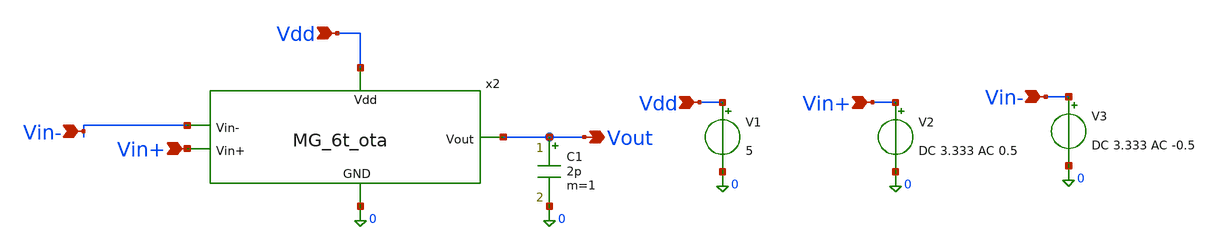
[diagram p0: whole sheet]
** sch_path: MG_6T_OTA/MG_6t_ota_testbench.sch
**.subckt MG_6t_ota_testbench Vdd Vin+ Vin- Vdd Vin+ Vin- Vout
*.ipin Vdd
*.ipin Vin+
*.ipin Vin-
*.ipin Vdd
*.ipin Vin+
*.ipin Vin-
*.opin Vout
V1 Vdd 0 5
V2 Vin+ 0 DC 3.333 AC 0.5
V3 Vin- 0 DC 3.333 AC -0.5
C1 Vout 0 2p m=1
x2 Vdd Vout Vin- Vin+ 0 MG_6t_ota
**** begin user architecture code



.include /foss/pdks/gf180mcuD/libs.tech/ngspice/design.ngspice
.lib /foss/pdks/gf180mcuD/libs.tech/ngspice/sm141064.ngspice typical
.lib /foss/pdks/gf180mcuD/libs.tech/ngspice/sm141064.ngspice res_typical
.lib /foss/pdks/gf180mcuD/libs.tech/ngspice/sm141064.ngspice moscap_typical
.lib /foss/pdks/gf180mcuD/libs.tech/ngspice/sm141064.ngspice diode_typical

.control
 save all
  op
  print all

  ac dec 10 1 1G
  meas ac dc_gain MAX vdb(Vout)
  meas ac ugbw WHEN vdb(Vout)=0 FALL=1
  let phase_deg = (180/PI)*vp(Vout)
  plot vdb(Vout)
  plot phase_deg
.endc


*.control
  *save all
  *op

  * ==========================================
  * 1. DIFFERENTIAL RUN (Adm & Noise)
  * ==========================================
  *alter v2 ac = 1
  *alter v3 ac = -1 ; Set this to 0 if v3 is just a DC reference

  *ac dec 20 1 1G
  *setplot ac1

  *let gain_db = vdb(vout)
  *let phase_deg = (180/PI) * ph(vout)
  *meas ac dc_gain MAX gain_db

  * Run Noise Analysis on the Differential Setup
  *noise v(vout) v2 dec 20 1 1G

  * ==========================================
  * 2. COMMON-MODE RUN (Acm)
  * ==========================================
  * Force both inputs to swing exactly the same way
  *alter v2 ac = 1
  *alter v3 ac = 1

  *ac dec 20 1 1G
  *setplot ac2
  *let cm_gain_db = vdb(vout)

  * ==========================================
  * 3. CMRR CALCULATION
  * ==========================================
  * CMRR = Differential Gain - Common Mode Gain
  *let cmrr_db = ac1.gain_db - ac2.cm_gain_db
  *meas ac max_cmrr MAX cmrr_db

  *print ac1.dc_gain max_cmrr

  * Plot everything together
  *plot ac1.gain_db ac2.cm_gain_db title 'Diff Gain vs CM Gain (dB)'
  *plot cmrr_db title 'CMRR (dB)'

  * =========================================
  * 4. NOISE CALCULATION
  * =========================================

  * Syntax: noise v(output_node) input_source dec points fstart fstop
  *noise v(vout) v2 dec 20 1 1G

  * ngspice creates 'noise1' for spectral density and 'noise2' for total noise
  *setplot noise1

  * Plot spectral densities (V/sqrt(Hz))
  *plot inoise_spectrum title 'Input Referred Noise Density'
  *plot onoise_spectrum title 'Output Referred Noise Density'

  * Calculate and print total integrated input RMS noise over the bandwidth
  *let total_in_noise = sqrt(integ(inoise_spectrum^2))
  *print total_in_noise


*.endc

*.include /foss/pdks/gf180mcuD/libs.tech/ngspice/design.ngspice

* MUST be defined here exactly as 1
*.param sw_stat_global=1
*.param sw_stat_mismatch=1

*.lib /foss/pdks/gf180mcuD/libs.tech/ngspice/sm141064.ngspice statistical
*.lib /foss/pdks/gf180mcuD/libs.tech/ngspice/sm141064.ngspice res_statistical
*.lib /foss/pdks/gf180mcuD/libs.tech/ngspice/sm141064.ngspice moscap_typical
*.lib /foss/pdks/gf180mcuD/libs.tech/ngspice/sm141064.ngspice diode_typical

*.control
*  let mc_runs = 50
*  let run_idx = 1

*  echo Run_Number DC_Gain_dB UGBW_Hz Phase_Margin_Deg > mc_results.txt

*  while run_idx <= mc_runs

    * 1. FLUSH THE CACHE: Turn off MC and reset
    * This forces NGSPICE to recognize a physical state change
*    alterparam sw_stat_global = 0
*    alterparam sw_stat_mismatch = 0
*    reset

    * 2. ROLL NEW DICE: Change seed, turn MC back on exactly to 1, and reset
    * Because the state changed from 0 -> 1, NGSPICE is forced to re-evaluate
    * the agauss() functions with the new seed!
*    setseed $&run_idx
*    alterparam sw_stat_global = 1
*    alterparam sw_stat_mismatch = 1
*    reset

*    op
*    print all


    * 3. Run Simulation
*    alter v2 ac = 1
*    ac dec 20 1 1G


    * 4. Measure
*    let gain_db = vdb(Vout)
*    let phase_deg = (180/PI) * ph(Vout)

*    meas ac dc_gain MAX gain_db
*    meas ac ugbw WHEN gain_db=0 FALL=1
*    meas ac ph_at_ugbw FIND phase_deg WHEN gain_db=0
*    let phase_margin = 180 + ph_at_ugbw

    * 5. Save data
*    echo $&run_idx $&dc_gain $&ugbw $&phase_margin >>
*+ /foss/designs/C05-MRTMOS-SSCS-Chipathon/MG_6T_OTA/plots_and_results/mc_results.txt

*    destroy all
*    let run_idx = run_idx + 1
*  end

*  echo Monte Carlo simulation complete check mc_results.txt
*.endc



**** end user architecture code
**.ends
.end
